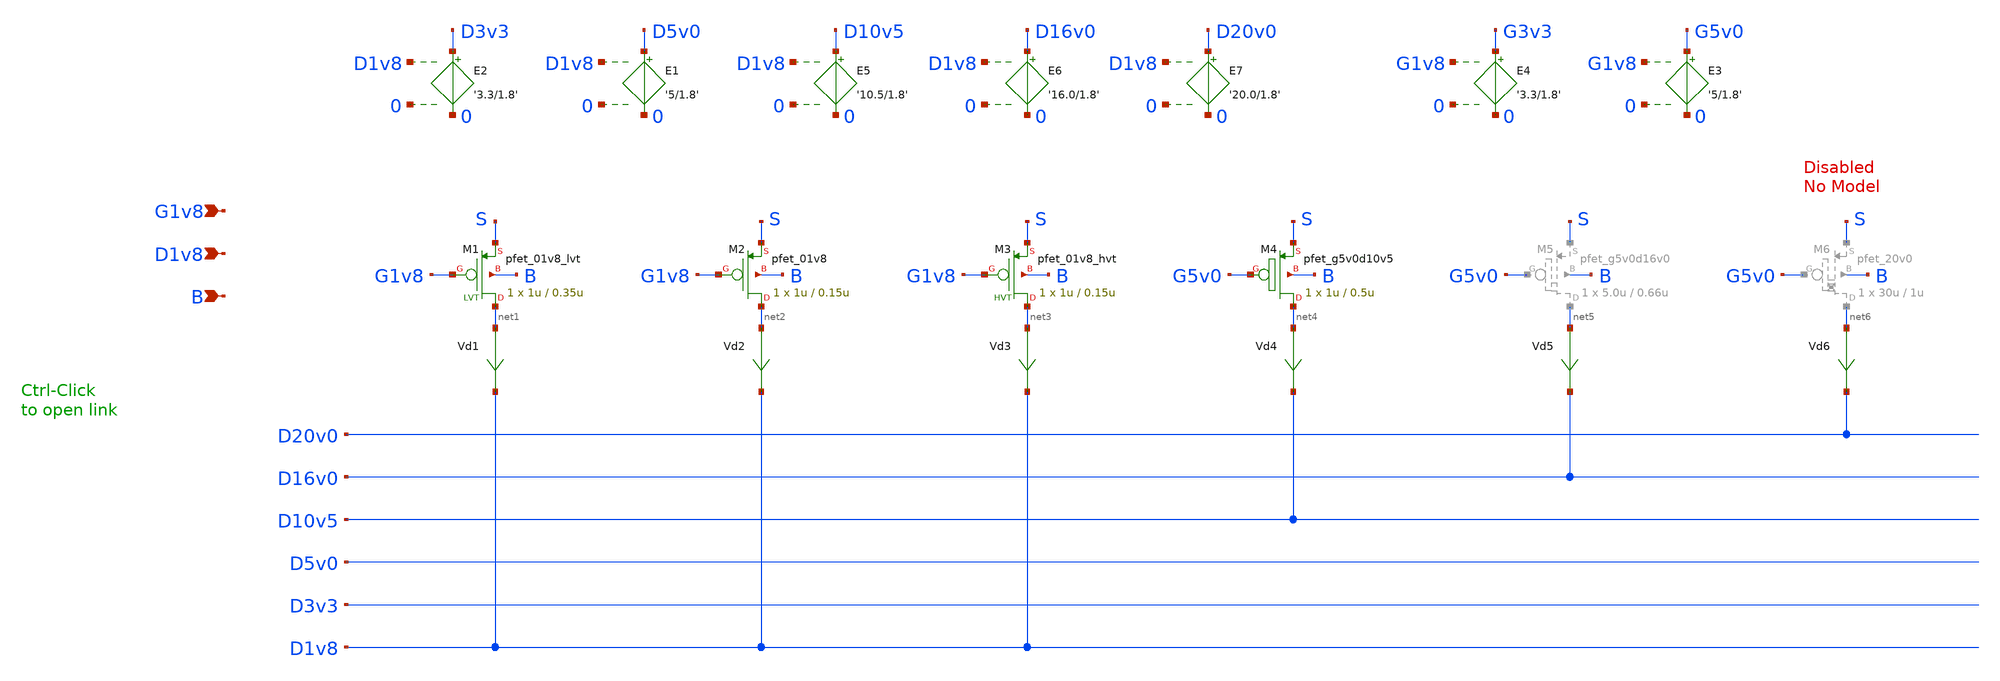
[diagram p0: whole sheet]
** sch_path: sky130_tests_X/test_pmos2x.sch
* Copyright 2020 Stefan Frederik Schippers
* Licensed under the Apache License, Version 2.0 (the "License");
* you may not use this file except in compliance with the License.
* You may obtain a copy of the License at
* https://www.apache.org/licenses/LICENSE-2.0
* Unless required by applicable law or agreed to in writing, software
* distributed under the License is distributed on an "AS IS" BASIS,
* WITHOUT WARRANTIES OR CONDITIONS OF ANY KIND, either express or implied.
* See the License for the specific language governing permissions and
* limitations under the License.
**.subckt test_pmos2x G1v8 D1v8 B
*.ipin G1v8
*.ipin D1v8
*.ipin B
Vd1 net1 D1v8 0
.save i(vd1)
Vd2 net2 D1v8 0
.save i(vd2)
E1 D5v0 0 D1v8 0 '5/1.8'
E2 D3v3 0 D1v8 0 '3.3/1.8'
E3 G5v0 0 G1v8 0 '5/1.8'
E4 G3v3 0 G1v8 0 '3.3/1.8'
E5 D10v5 0 D1v8 0 '10.5/1.8'
Vd3 net3 D1v8 0
.save i(vd3)
Vd4 net4 D10v5 0
.save i(vd4)
Vd5 net5 D16v0 0
.save i(vd5)
E6 D16v0 0 D1v8 0 '16.0/1.8'
E7 D20v0 0 D1v8 0 '20.0/1.8'
Vd6 net6 D20v0 0
.save i(vd6)
XM1 net1 G1v8 S B sky130_fd_pr__pfet_01v8_lvt w=1u l=0.35u ad=[sky130_fet_ad_cb 1u ]
+ pd=[sky130_fet_pd_cb 1u ] as=[sky130_fet_ad_cb 1u ] ps=[sky130_fet_pd_cb 1u ] nrd=[sky130_fet_nrd_cb 1u ]
+ nrs=[sky130_fet_nrd_cb 1u ] sa=0 sb=0 sd=0 nf=1 mult=1 m=1
XM2 net2 G1v8 S B sky130_fd_pr__pfet_01v8 w=1u l=0.15u ad=[sky130_fet_ad_cb 1u ]
+ pd=[sky130_fet_pd_cb 1u ] as=[sky130_fet_ad_cb 1u ] ps=[sky130_fet_pd_cb 1u ] nrd=[sky130_fet_nrd_cb 1u ]
+ nrs=[sky130_fet_nrd_cb 1u ] sa=0 sb=0 sd=0 nf=1 mult=1 m=1
XM3 net3 G1v8 S B sky130_fd_pr__pfet_01v8_hvt w=1u l=0.15u ad=[sky130_fet_ad_cb 1u ]
+ pd=[sky130_fet_pd_cb 1u ] as=[sky130_fet_ad_cb 1u ] ps=[sky130_fet_pd_cb 1u ] nrd=[sky130_fet_nrd_cb 1u ]
+ nrs=[sky130_fet_nrd_cb 1u ] sa=0 sb=0 sd=0 nf=1 mult=1 m=1
XM4 net4 G5v0 S B sky130_fd_pr__pfet_g5v0d10v5 w=1u l=0.5u ad=[sky130_fet_ad_cb 1u ]
+ pd=[sky130_fet_pd_cb 1u ] as=[sky130_fet_ad_cb 1u ] ps=[sky130_fet_pd_cb 1u ] nrd=[sky130_fet_nrd_cb 1u ]
+ nrs=[sky130_fet_nrd_cb 1u ] sa=0 sb=0 sd=0 nf=1 mult=1 m=1
**** begin user architecture code


vg 0 G1v8 0
vs s 0 0
vd 0 D1v8 0
vb b 0 0
.dc vd 0 1.8 0.01
.step vg 0 1.8 0.2
.options parser model_binning=true
.print dc format=raw I(vd1) I(vd2) I(vd3) I(vd4)



**** end user architecture code
**.ends
.end
